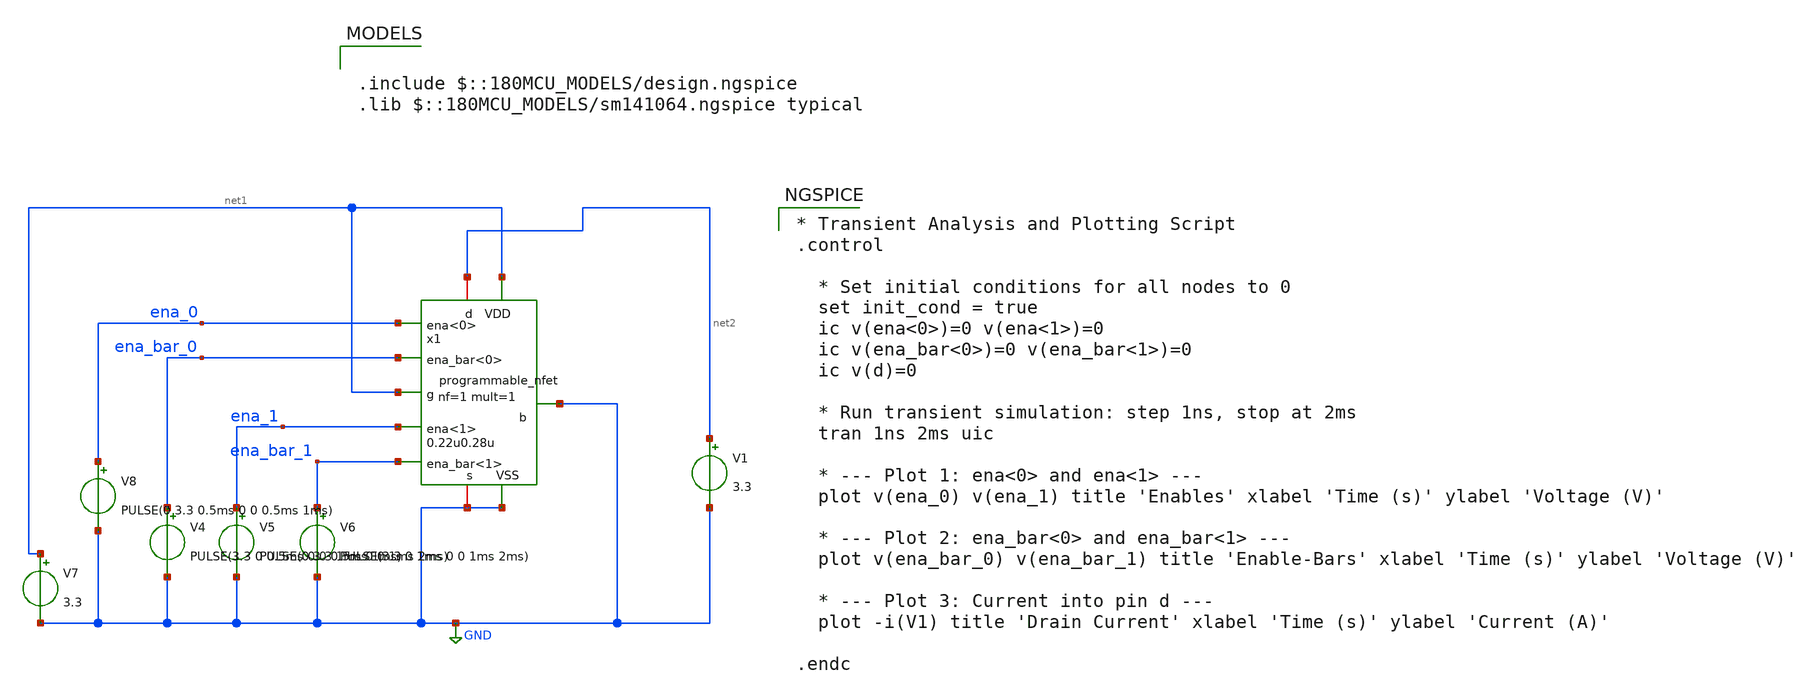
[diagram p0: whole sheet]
** sch_path: designs/libs/core_digital/tb/TB_prog_fet.sch
**.subckt TB_prog_fet
V4 ena_bar_0 GND PULSE(3.3 0 0.5ms 0 0 0.5ms 1ms)
V5 ena_1 GND PULSE(0 3.3 1ms 0 0 1ms 2ms)
V6 ena_bar_1 GND PULSE(3.3 0 1ms 0 0 1ms 2ms)
V7 net1 GND 3.3
V8 ena_0 GND PULSE(0 3.3 0.5ms 0 0 0.5ms 1ms)
V1 net2 GND 3.3
x1 net2 GND net1 GND ena_bar_0 net1 ena_bar_1 ena_0 ena_1 GND programmable_nfet width=0.22u
+ length=0.28u nf=1 mult=1
**** begin user architecture code

.include $::180MCU_MODELS/design.ngspice
.lib $::180MCU_MODELS/sm141064.ngspice typical


* Transient Analysis and Plotting Script
.control

  * Set initial conditions for all nodes to 0
  set init_cond = true
  ic v(ena<0>)=0 v(ena<1>)=0
  ic v(ena_bar<0>)=0 v(ena_bar<1>)=0
  ic v(d)=0

  * Run transient simulation: step 1ns, stop at 2ms
  tran 1ns 2ms uic

  * --- Plot 1: ena<0> and ena<1> ---
  plot v(ena_0) v(ena_1) title 'Enables' xlabel 'Time (s)' ylabel 'Voltage (V)'

  * --- Plot 2: ena_bar<0> and ena_bar<1> ---
  plot v(ena_bar_0) v(ena_bar_1) title 'Enable-Bars' xlabel 'Time (s)' ylabel 'Voltage (V)'

  * --- Plot 3: Current into pin d ---
  plot -i(V1) title 'Drain Current' xlabel 'Time (s)' ylabel 'Current (A)'

.endc

**** end user architecture code
**.ends

* expanding   symbol:  libs/core_digital/schem/programmable_nfet.sym # of pins=10
** sym_path: designs/libs/core_digital/schem/programmable_nfet.sym
** sch_path: designs/libs/core_digital/schem/programmable_nfet.sch
.subckt programmable_nfet d b g s ena_bar<0> VDD ena_bar<1> ena<0> ena<1> VSS  width=0.22u
+ length=0.28u nf=1 mult=1
*.ipin VSS
*.ipin VDD
*.ipin g
*.ipin ena_bar<1>
*.ipin ena_bar<0>
*.ipin ena<1>
*.ipin ena<0>
*.iopin d
*.iopin s
*.ipin b
XM1 d net2 s b nfet_03v3 L={length} W={width} nf={nf} ad='int((nf+1)/2) * W/nf * 0.18u' as='int((nf+2)/2) * W/nf * 0.18u'
+ pd='2*int((nf+1)/2) * (W/nf + 0.18u)' ps='2*int((nf+2)/2) * (W/nf + 0.18u)' nrd='0.18u / W' nrs='0.18u / W'
+ sa=0 sb=0 sd=0 m={mult}
XM3 d net1 s b nfet_03v3 L={length} W={2*width} nf={2*nf} ad='int((nf+1)/2) * W/nf * 0.18u' as='int((nf+2)/2) * W/nf * 0.18u'
+ pd='2*int((nf+1)/2) * (W/nf + 0.18u)' ps='2*int((nf+2)/2) * (W/nf + 0.18u)' nrd='0.18u / W' nrs='0.18u / W'
+ sa=0 sb=0 sd=0 m={mult}
XM2 net1 ena_bar<1> VSS VSS nfet_03v3 L=0.28u W=0.22u nf=1 ad='int((nf+1)/2) * W/nf * 0.18u' as='int((nf+2)/2) * W/nf * 0.18u'
+ pd='2*int((nf+1)/2) * (W/nf + 0.18u)' ps='2*int((nf+2)/2) * (W/nf + 0.18u)' nrd='0.18u / W' nrs='0.18u / W'
+ sa=0 sb=0 sd=0 m=1
XM4 net2 ena_bar<0> VSS VSS nfet_03v3 L=0.28u W=0.22u nf=1 ad='int((nf+1)/2) * W/nf * 0.18u' as='int((nf+2)/2) * W/nf * 0.18u'
+ pd='2*int((nf+1)/2) * (W/nf + 0.18u)' ps='2*int((nf+2)/2) * (W/nf + 0.18u)' nrd='0.18u / W' nrs='0.18u / W'
+ sa=0 sb=0 sd=0 m=1
x1 ena_bar<0> VDD net2 g VSS ena<0> transmission_gate
x2 ena_bar<1> VDD net1 g VSS ena<1> transmission_gate
.ends


* expanding   symbol:  libs/core_digital/schem/transmission_gate.sym # of pins=6
** sym_path: designs/libs/core_digital/schem/transmission_gate.sym
** sch_path: designs/libs/core_digital/schem/transmission_gate.sch
.subckt transmission_gate ena_bar VDD out in VSS ena
*.ipin in
*.ipin ena_bar
*.ipin ena
*.ipin VSS
*.ipin VDD
*.opin out
XM1 in ena_bar out VDD pfet_03v3 L=0.28u W=0.22u nf=1 ad='int((nf+1)/2) * W/nf * 0.18u' as='int((nf+2)/2) * W/nf * 0.18u'
+ pd='2*int((nf+1)/2) * (W/nf + 0.18u)' ps='2*int((nf+2)/2) * (W/nf + 0.18u)' nrd='0.18u / W' nrs='0.18u / W'
+ sa=0 sb=0 sd=0 m=1
XM2 in ena out VSS nfet_03v3 L=0.28u W=0.22u nf=1 ad='int((nf+1)/2) * W/nf * 0.18u' as='int((nf+2)/2) * W/nf * 0.18u'
+ pd='2*int((nf+1)/2) * (W/nf + 0.18u)' ps='2*int((nf+2)/2) * (W/nf + 0.18u)' nrd='0.18u / W' nrs='0.18u / W'
+ sa=0 sb=0 sd=0 m=1
.ends

.GLOBAL GND
.end
